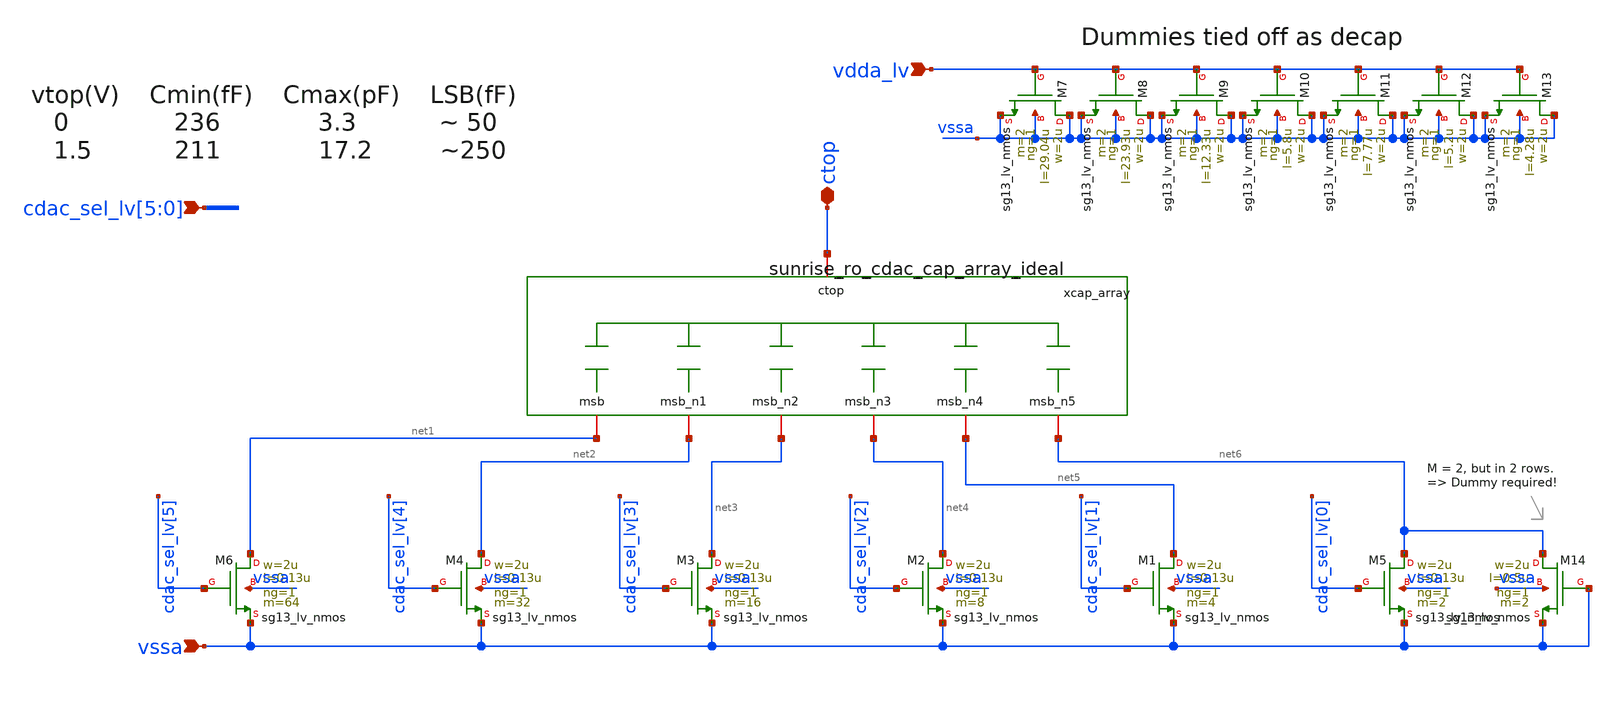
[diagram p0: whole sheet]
** sch_path: Schematics_Layout/sunrise_ro_cdac/sunrise_ro_cdac.sch
**.subckt sunrise_ro_cdac
*+ cdac_sel_lv[5],cdac_sel_lv[4],cdac_sel_lv[3],cdac_sel_lv[2],cdac_sel_lv[1],cdac_sel_lv[0] vssa ctop vdda_lv
*.ipin cdac_sel_lv[5],cdac_sel_lv[4],cdac_sel_lv[3],cdac_sel_lv[2],cdac_sel_lv[1],cdac_sel_lv[0]
*.ipin vssa
*.iopin ctop
*.ipin vdda_lv
xcap_array ctop net3 net4 net5 net6 net2 net1 sunrise_ro_cdac_cap_array_ideal
XM5 net6 cdac_sel_lv[0] vssa vssa sg13_lv_nmos w=2u l=0.13u ng=1 m=2 mm_ok=1
XM1 net5 cdac_sel_lv[1] vssa vssa sg13_lv_nmos w=2u l=0.13u ng=1 m=4 mm_ok=1
XM2 net4 cdac_sel_lv[2] vssa vssa sg13_lv_nmos w=2u l=0.13u ng=1 m=8 mm_ok=1
XM3 net3 cdac_sel_lv[3] vssa vssa sg13_lv_nmos w=2u l=0.13u ng=1 m=16 mm_ok=1
XM4 net2 cdac_sel_lv[4] vssa vssa sg13_lv_nmos w=2u l=0.13u ng=1 m=32 mm_ok=1
XM6 net1 cdac_sel_lv[5] vssa vssa sg13_lv_nmos w=2u l=0.13u ng=1 m=64 mm_ok=1
XM7 vssa vdda_lv vssa vssa sg13_lv_nmos w=2u l=29.04u ng=1 m=2 mm_ok=1
XM8 vssa vdda_lv vssa vssa sg13_lv_nmos w=2u l=23.93u ng=1 m=2 mm_ok=1
XM9 vssa vdda_lv vssa vssa sg13_lv_nmos w=2u l=12.33u ng=1 m=2 mm_ok=1
XM10 vssa vdda_lv vssa vssa sg13_lv_nmos w=2u l=5.8u ng=1 m=2 mm_ok=1
XM11 vssa vdda_lv vssa vssa sg13_lv_nmos w=2u l=7.77u ng=1 m=2 mm_ok=1
XM12 vssa vdda_lv vssa vssa sg13_lv_nmos w=2u l=5.2u ng=1 m=2 mm_ok=1
XM13 vssa vdda_lv vssa vssa sg13_lv_nmos w=2u l=4.28u ng=1 m=2 mm_ok=1
XM14 net6 vssa vssa vssa sg13_lv_nmos w=2u l=0.5u ng=1 m=2 mm_ok=1
**.ends
.end
